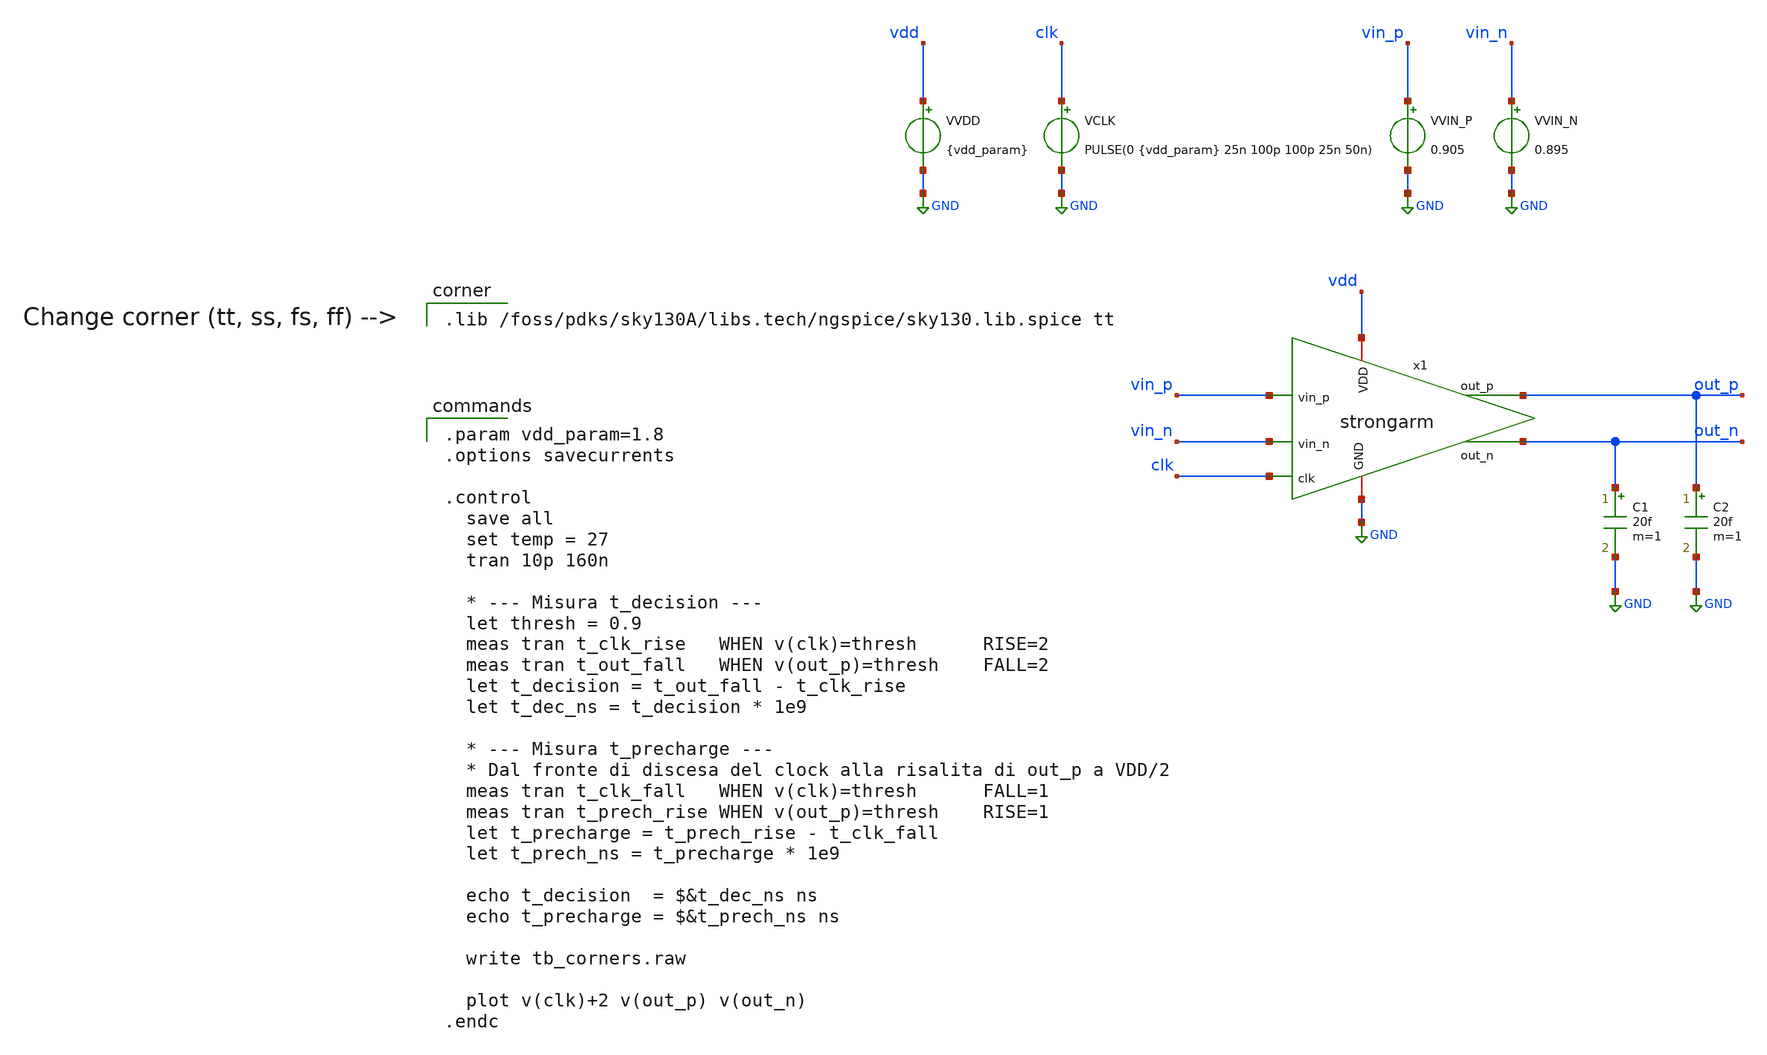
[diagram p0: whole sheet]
** sch_path: 01_xschem_ngspice/soluzioni/lab03/xschem/tb_corners.sch
**.subckt tb_corners
x1 vdd out_p out_n vin_p vin_n clk GND strongarm
VVDD vdd GND {vdd_param}
VCLK clk GND PULSE(0 {vdd_param} 25n 100p 100p 25n 50n)
VVIN_P vin_p GND 0.905
VVIN_N vin_n GND 0.895
C1 out_n GND 20f m=1
C2 out_p GND 20f m=1
**** begin user architecture code

.lib /foss/pdks/sky130A/libs.tech/ngspice/sky130.lib.spice tt


.param vdd_param=1.8
.options savecurrents

.control
  save all
  set temp = 27
  tran 10p 160n

  * --- Misura t_decision ---
  let thresh = 0.9
  meas tran t_clk_rise   WHEN v(clk)=thresh      RISE=2
  meas tran t_out_fall   WHEN v(out_p)=thresh    FALL=2
  let t_decision = t_out_fall - t_clk_rise
  let t_dec_ns = t_decision * 1e9

  * --- Misura t_precharge ---
  * Dal fronte di discesa del clock alla risalita di out_p a VDD/2
  meas tran t_clk_fall   WHEN v(clk)=thresh      FALL=1
  meas tran t_prech_rise WHEN v(out_p)=thresh    RISE=1
  let t_precharge = t_prech_rise - t_clk_fall
  let t_prech_ns = t_precharge * 1e9

  echo t_decision  = $&t_dec_ns ns
  echo t_precharge = $&t_prech_ns ns

  write tb_corners.raw

  plot v(clk)+2 v(out_p) v(out_n)
.endc

**** end user architecture code
**.ends
.GLOBAL GND
.end
